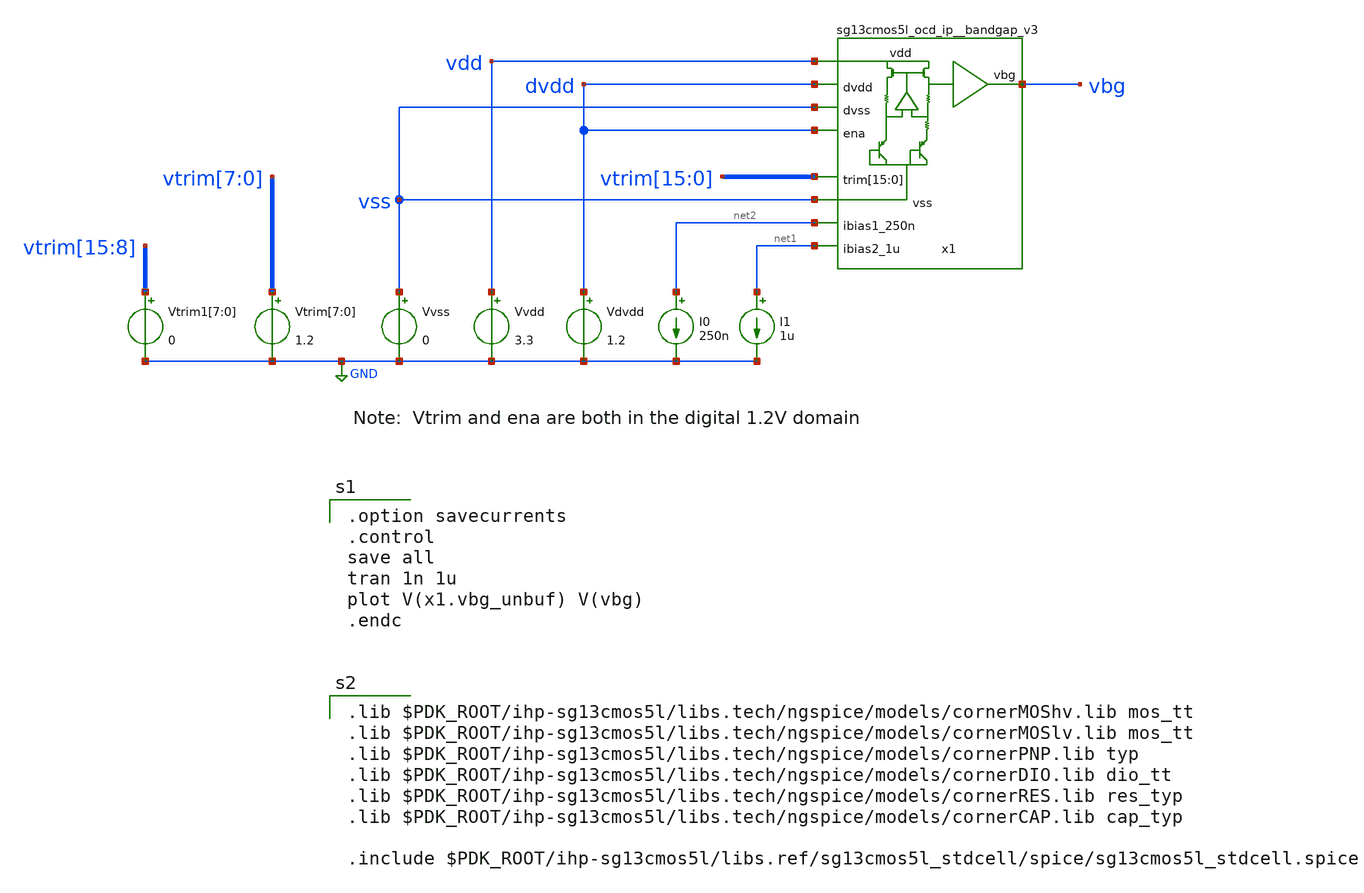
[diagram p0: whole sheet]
** sch_path: xschem/bandgap_tb.sch
**.subckt bandgap_tb
Vvss vss GND 0
Vtrim[7] vtrim[7] GND 1.2
Vtrim[6] vtrim[6] GND 1.2
Vtrim[5] vtrim[5] GND 1.2
Vtrim[4] vtrim[4] GND 1.2
Vtrim[3] vtrim[3] GND 1.2
Vtrim[2] vtrim[2] GND 1.2
Vtrim[1] vtrim[1] GND 1.2
Vtrim[0] vtrim[0] GND 1.2
Vvdd vdd GND 3.3
I0 net2 GND 250n
Vdvdd dvdd GND 1.2
I1 net1 GND 1u
Vtrim1[7] vtrim[15] GND 0
Vtrim1[6] vtrim[14] GND 0
Vtrim1[5] vtrim[13] GND 0
Vtrim1[4] vtrim[12] GND 0
Vtrim1[3] vtrim[11] GND 0
Vtrim1[2] vtrim[10] GND 0
Vtrim1[1] vtrim[9] GND 0
Vtrim1[0] vtrim[8] GND 0
x1 vdd vbg vss net2 vtrim[15] vtrim[14] vtrim[13] vtrim[12] vtrim[11] vtrim[10] vtrim[9] vtrim[8]
+ vtrim[7] vtrim[6] vtrim[5] vtrim[4] vtrim[3] vtrim[2] vtrim[1] vtrim[0] vss dvdd dvdd net1
+ sg13cmos5l_ocd_ip__bandgap_v3
**** begin user architecture code

.option savecurrents
.control
save all
tran 1n 1u
plot V(x1.vbg_unbuf) V(vbg)
.endc


.lib $PDK_ROOT/ihp-sg13cmos5l/libs.tech/ngspice/models/cornerMOShv.lib mos_tt
.lib $PDK_ROOT/ihp-sg13cmos5l/libs.tech/ngspice/models/cornerMOSlv.lib mos_tt
.lib $PDK_ROOT/ihp-sg13cmos5l/libs.tech/ngspice/models/cornerPNP.lib typ
.lib $PDK_ROOT/ihp-sg13cmos5l/libs.tech/ngspice/models/cornerDIO.lib dio_tt
.lib $PDK_ROOT/ihp-sg13cmos5l/libs.tech/ngspice/models/cornerRES.lib res_typ
.lib $PDK_ROOT/ihp-sg13cmos5l/libs.tech/ngspice/models/cornerCAP.lib cap_typ

.include $PDK_ROOT/ihp-sg13cmos5l/libs.ref/sg13cmos5l_stdcell/spice/sg13cmos5l_stdcell.spice


**** end user architecture code
**.ends
.GLOBAL GND
.end
